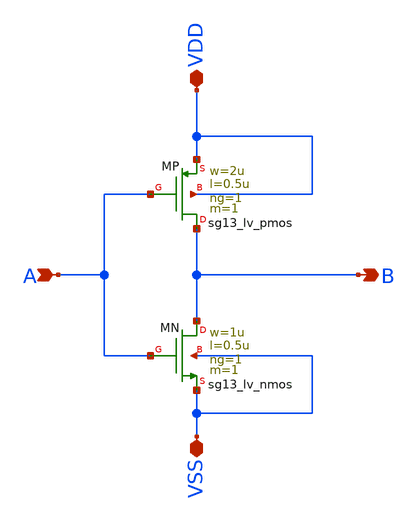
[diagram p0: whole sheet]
** sch_path: work/gate_inv_L0d5/xschem/gate_inv_L0d5.sch
**.subckt gate_inv_L0d5 B A VDD VSS
*.opin B
*.ipin A
*.iopin VDD
*.iopin VSS
XMN B A VSS VSS sg13_lv_nmos w=1u l=0.5u ng=1 m=1 mm_ok=1
XMP B A VDD VDD sg13_lv_pmos w=2u l=0.5u ng=1 m=1 mm_ok=1
**.ends
.end
